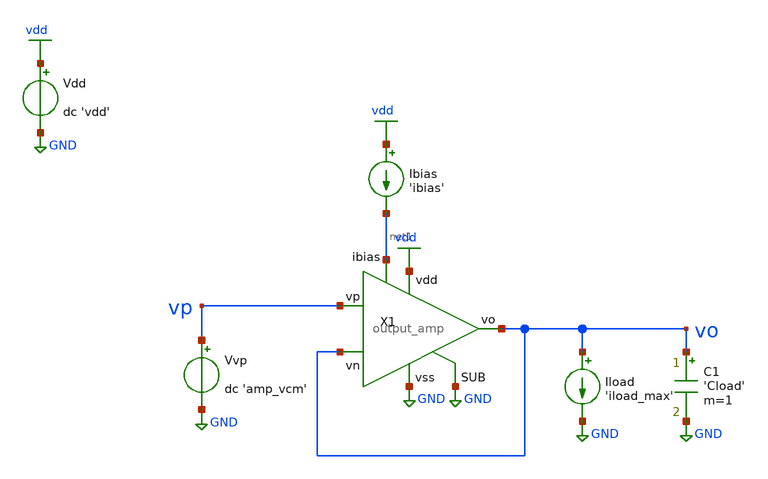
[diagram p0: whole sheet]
** sch_path: tb/output_amp/tb_amp_load_reg.sch
**.subckt tb_amp_load_reg
X1 vdd vo vp vo net1 GND GND output_amp
Vdd vdd GND dc 'vdd'
Vvp vp GND dc 'amp_vcm'
Ibias vdd net1 'ibias'
C1 vo GND 'Cload' m=1
Iload vo GND 'iload_max'
**** begin user architecture code


.lib 'models_dir'/cornerMOShv.lib 'mos_corner'
.lib 'models_dir'/cornerCAP.lib cap_typ
.option TEMP='temperature'
.option warn=1
.control
save all
dc Iload 'iload_min' 'iload_max' 1n
set wr_singlescale
wrdata 'simpath'/'filename'_'N'.data V(vo)
quit
.endc


**** end user architecture code
**.ends
.GLOBAL GND
.GLOBAL vdd
.end
